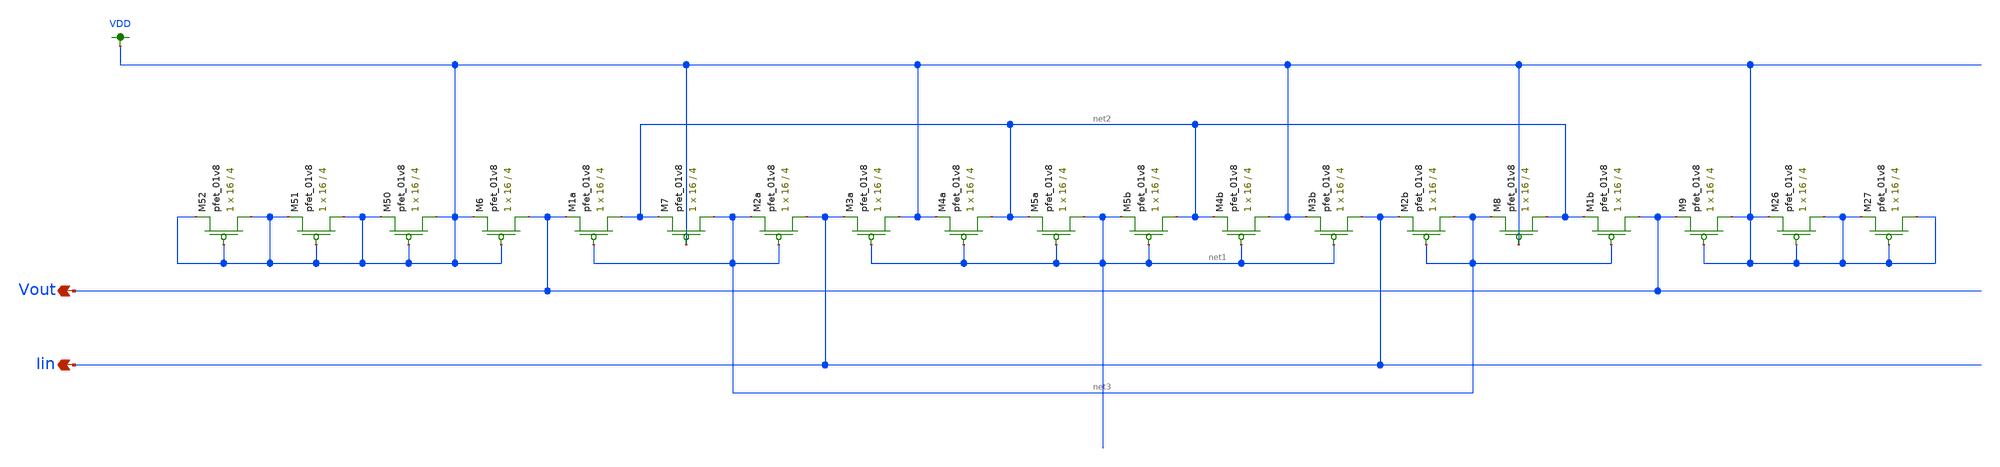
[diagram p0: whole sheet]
** sch_path: schematic/LDS/low-voltage_super-wilson_LDS_pmos.sch
**.subckt low-voltage_super-wilson_LDS_pmos Vout Iin
*.opin Vout
*.opin Iin
XM7 net3 VDD net2 VDD sky130_fd_pr__pfet_01v8 L=4 W=16 nf=1 ad='int((nf+1)/2) * W/nf * 0.29' as='int((nf+2)/2) * W/nf * 0.29'
+ pd='2*int((nf+1)/2) * (W/nf + 0.29)' ps='2*int((nf+2)/2) * (W/nf + 0.29)' nrd='0.29 / W' nrs='0.29 / W'
+ sa=0 sb=0 sd=0 mult=1 m=1
XM2a Iin net3 net3 VDD sky130_fd_pr__pfet_01v8 L=4 W=16 nf=1 ad='int((nf+1)/2) * W/nf * 0.29' as='int((nf+2)/2) * W/nf * 0.29'
+ pd='2*int((nf+1)/2) * (W/nf + 0.29)' ps='2*int((nf+2)/2) * (W/nf + 0.29)' nrd='0.29 / W' nrs='0.29 / W'
+ sa=0 sb=0 sd=0 mult=1 m=1
XM3a VDD net1 Iin VDD sky130_fd_pr__pfet_01v8 L=4 W=16 nf=1 ad='int((nf+1)/2) * W/nf * 0.29' as='int((nf+2)/2) * W/nf * 0.29'
+ pd='2*int((nf+1)/2) * (W/nf + 0.29)' ps='2*int((nf+2)/2) * (W/nf + 0.29)' nrd='0.29 / W' nrs='0.29 / W'
+ sa=0 sb=0 sd=0 mult=1 m=1
XM4a net2 net1 VDD VDD sky130_fd_pr__pfet_01v8 L=4 W=16 nf=1 ad='int((nf+1)/2) * W/nf * 0.29' as='int((nf+2)/2) * W/nf * 0.29'
+ pd='2*int((nf+1)/2) * (W/nf + 0.29)' ps='2*int((nf+2)/2) * (W/nf + 0.29)' nrd='0.29 / W' nrs='0.29 / W'
+ sa=0 sb=0 sd=0 mult=1 m=1
XM5a net1 net1 net2 VDD sky130_fd_pr__pfet_01v8 L=4 W=16 nf=1 ad='int((nf+1)/2) * W/nf * 0.29' as='int((nf+2)/2) * W/nf * 0.29'
+ pd='2*int((nf+1)/2) * (W/nf + 0.29)' ps='2*int((nf+2)/2) * (W/nf + 0.29)' nrd='0.29 / W' nrs='0.29 / W'
+ sa=0 sb=0 sd=0 mult=1 m=1
XM5b net2 net1 net1 VDD sky130_fd_pr__pfet_01v8 L=4 W=16 nf=1 ad='int((nf+1)/2) * W/nf * 0.29' as='int((nf+2)/2) * W/nf * 0.29'
+ pd='2*int((nf+1)/2) * (W/nf + 0.29)' ps='2*int((nf+2)/2) * (W/nf + 0.29)' nrd='0.29 / W' nrs='0.29 / W'
+ sa=0 sb=0 sd=0 mult=1 m=1
XM4b VDD net1 net2 VDD sky130_fd_pr__pfet_01v8 L=4 W=16 nf=1 ad='int((nf+1)/2) * W/nf * 0.29' as='int((nf+2)/2) * W/nf * 0.29'
+ pd='2*int((nf+1)/2) * (W/nf + 0.29)' ps='2*int((nf+2)/2) * (W/nf + 0.29)' nrd='0.29 / W' nrs='0.29 / W'
+ sa=0 sb=0 sd=0 mult=1 m=1
XM3b Iin net1 VDD VDD sky130_fd_pr__pfet_01v8 L=4 W=16 nf=1 ad='int((nf+1)/2) * W/nf * 0.29' as='int((nf+2)/2) * W/nf * 0.29'
+ pd='2*int((nf+1)/2) * (W/nf + 0.29)' ps='2*int((nf+2)/2) * (W/nf + 0.29)' nrd='0.29 / W' nrs='0.29 / W'
+ sa=0 sb=0 sd=0 mult=1 m=1
XM2b net3 net3 Iin VDD sky130_fd_pr__pfet_01v8 L=4 W=16 nf=1 ad='int((nf+1)/2) * W/nf * 0.29' as='int((nf+2)/2) * W/nf * 0.29'
+ pd='2*int((nf+1)/2) * (W/nf + 0.29)' ps='2*int((nf+2)/2) * (W/nf + 0.29)' nrd='0.29 / W' nrs='0.29 / W'
+ sa=0 sb=0 sd=0 mult=1 m=1
XM8 net2 VDD net3 VDD sky130_fd_pr__pfet_01v8 L=4 W=16 nf=1 ad='int((nf+1)/2) * W/nf * 0.29' as='int((nf+2)/2) * W/nf * 0.29'
+ pd='2*int((nf+1)/2) * (W/nf + 0.29)' ps='2*int((nf+2)/2) * (W/nf + 0.29)' nrd='0.29 / W' nrs='0.29 / W'
+ sa=0 sb=0 sd=0 mult=1 m=1
XM1a net2 net3 Vout VDD sky130_fd_pr__pfet_01v8 L=4 W=16 nf=1 ad='int((nf+1)/2) * W/nf * 0.29' as='int((nf+2)/2) * W/nf * 0.29'
+ pd='2*int((nf+1)/2) * (W/nf + 0.29)' ps='2*int((nf+2)/2) * (W/nf + 0.29)' nrd='0.29 / W' nrs='0.29 / W'
+ sa=0 sb=0 sd=0 mult=1 m=1
XM1b Vout net3 net2 VDD sky130_fd_pr__pfet_01v8 L=4 W=16 nf=1 ad='int((nf+1)/2) * W/nf * 0.29' as='int((nf+2)/2) * W/nf * 0.29'
+ pd='2*int((nf+1)/2) * (W/nf + 0.29)' ps='2*int((nf+2)/2) * (W/nf + 0.29)' nrd='0.29 / W' nrs='0.29 / W'
+ sa=0 sb=0 sd=0 mult=1 m=1
XM6 Vout VDD VDD VDD sky130_fd_pr__pfet_01v8 L=4 W=16 nf=1 ad='int((nf+1)/2) * W/nf * 0.29' as='int((nf+2)/2) * W/nf * 0.29'
+ pd='2*int((nf+1)/2) * (W/nf + 0.29)' ps='2*int((nf+2)/2) * (W/nf + 0.29)' nrd='0.29 / W' nrs='0.29 / W'
+ sa=0 sb=0 sd=0 mult=1 m=1
XM9 VDD VDD Vout VDD sky130_fd_pr__pfet_01v8 L=4 W=16 nf=1 ad='int((nf+1)/2) * W/nf * 0.29' as='int((nf+2)/2) * W/nf * 0.29'
+ pd='2*int((nf+1)/2) * (W/nf + 0.29)' ps='2*int((nf+2)/2) * (W/nf + 0.29)' nrd='0.29 / W' nrs='0.29 / W'
+ sa=0 sb=0 sd=0 mult=1 m=1
XM26 VDD VDD VDD VDD sky130_fd_pr__pfet_01v8 L=4 W=16 nf=1 ad='int((nf+1)/2) * W/nf * 0.29' as='int((nf+2)/2) * W/nf * 0.29'
+ pd='2*int((nf+1)/2) * (W/nf + 0.29)' ps='2*int((nf+2)/2) * (W/nf + 0.29)' nrd='0.29 / W' nrs='0.29 / W'
+ sa=0 sb=0 sd=0 mult=1 m=1
XM27 VDD VDD VDD VDD sky130_fd_pr__pfet_01v8 L=4 W=16 nf=1 ad='int((nf+1)/2) * W/nf * 0.29' as='int((nf+2)/2) * W/nf * 0.29'
+ pd='2*int((nf+1)/2) * (W/nf + 0.29)' ps='2*int((nf+2)/2) * (W/nf + 0.29)' nrd='0.29 / W' nrs='0.29 / W'
+ sa=0 sb=0 sd=0 mult=1 m=1
XM50 VDD VDD VDD VDD sky130_fd_pr__pfet_01v8 L=4 W=16 nf=1 ad='int((nf+1)/2) * W/nf * 0.29' as='int((nf+2)/2) * W/nf * 0.29'
+ pd='2*int((nf+1)/2) * (W/nf + 0.29)' ps='2*int((nf+2)/2) * (W/nf + 0.29)' nrd='0.29 / W' nrs='0.29 / W'
+ sa=0 sb=0 sd=0 mult=1 m=1
XM51 VDD VDD VDD VDD sky130_fd_pr__pfet_01v8 L=4 W=16 nf=1 ad='int((nf+1)/2) * W/nf * 0.29' as='int((nf+2)/2) * W/nf * 0.29'
+ pd='2*int((nf+1)/2) * (W/nf + 0.29)' ps='2*int((nf+2)/2) * (W/nf + 0.29)' nrd='0.29 / W' nrs='0.29 / W'
+ sa=0 sb=0 sd=0 mult=1 m=1
XM52 VDD VDD VDD VDD sky130_fd_pr__pfet_01v8 L=4 W=16 nf=1 ad='int((nf+1)/2) * W/nf * 0.29' as='int((nf+2)/2) * W/nf * 0.29'
+ pd='2*int((nf+1)/2) * (W/nf + 0.29)' ps='2*int((nf+2)/2) * (W/nf + 0.29)' nrd='0.29 / W' nrs='0.29 / W'
+ sa=0 sb=0 sd=0 mult=1 m=1
**.ends
.GLOBAL VDD
.end
